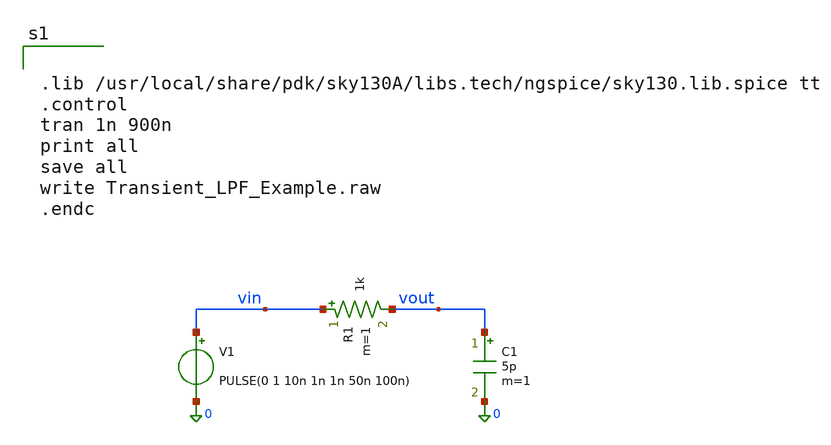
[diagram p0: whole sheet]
** sch_path: mag/layout/Transient_LPF_Example.sch
**.subckt Transient_LPF_Example
V1 vin 0 PULSE(0 1 10n 1n 1n 50n 100n)
R1 vin vout 1k m=1
C1 vout 0 5p m=1
**** begin user architecture code


.lib /usr/local/share/pdk/sky130A/libs.tech/ngspice/sky130.lib.spice tt
.control
tran 1n 900n
print all
save all
write Transient_LPF_Example.raw
.endc

**** end user architecture code
**.ends
.end
